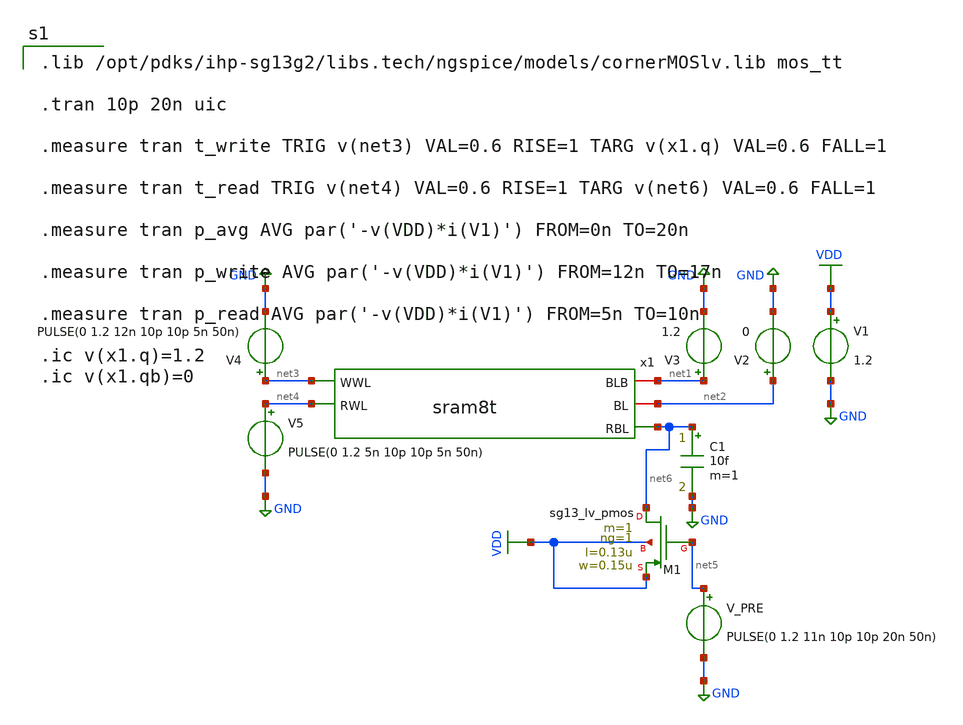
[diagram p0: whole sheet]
** sch_path: sram8t/schematic/sram8t_tb.sch
**.subckt sram8t_tb
V1 VDD GND 1.2
V3 net1 GND 1.2
V2 net2 GND 0
V4 net3 GND PULSE(0 1.2 12n 10p 10p 5n 50n)
V5 net4 GND PULSE(0 1.2 5n 10p 10p 5n 50n)
x1 net1 net2 net3 net6 net4 sram8t
XM1 net6 net5 VDD VDD sg13_lv_pmos w=0.15u l=0.13u ng=1 m=1 mm_ok=1
V_PRE net5 GND PULSE(0 1.2 11n 10p 10p 20n 50n)
C1 net6 GND 10f m=1
**** begin user architecture code

.lib /opt/pdks/ihp-sg13g2/libs.tech/ngspice/models/cornerMOSlv.lib mos_tt

.tran 10p 20n uic

.measure tran t_write TRIG v(net3) VAL=0.6 RISE=1 TARG v(x1.q) VAL=0.6 FALL=1

.measure tran t_read TRIG v(net4) VAL=0.6 RISE=1 TARG v(net6) VAL=0.6 FALL=1

.measure tran p_avg AVG par('-v(VDD)*i(V1)') FROM=0n TO=20n

.measure tran p_write AVG par('-v(VDD)*i(V1)') FROM=12n TO=17n

.measure tran p_read AVG par('-v(VDD)*i(V1)') FROM=5n TO=10n

.ic v(x1.q)=1.2
.ic v(x1.qb)=0

**** end user architecture code
**.ends

* expanding   symbol:  sram8t.sym # of pins=5
** sym_path: sram8t/schematic/sram8t.sym
** sch_path: sram8t/schematic/sram8t.sch
.subckt sram8t BLB BL WWL RBL RWL
*.iopin BL
*.iopin BLB
*.ipin WWL
*.ipin RWL
*.opin RBL
XM1 Q QB GND GND sg13_lv_nmos w=0.15u l=0.13u ng=1 m=1 mm_ok=1
XM2 QB Q GND GND sg13_lv_nmos w=0.15u l=0.13u ng=1 m=1 mm_ok=1
XM3 Q QB VDD VDD sg13_lv_pmos w=0.15u l=0.13u ng=1 m=1 mm_ok=1
XM4 QB Q VDD VDD sg13_lv_pmos w=0.15u l=0.13u ng=1 m=1 mm_ok=1
XM5 Q WWL BL GND sg13_lv_nmos w=0.15u l=0.13u ng=1 m=1 mm_ok=1
XM6 QB WWL BLB GND sg13_lv_nmos w=0.15u l=0.13u ng=1 m=1 mm_ok=1
XM7 RBL RWL net1 GND sg13_lv_nmos w=0.15u l=0.13u ng=1 m=1 mm_ok=1
XM8 net1 Q GND GND sg13_lv_nmos w=0.15u l=0.13u ng=1 m=1 mm_ok=1
.ends

.GLOBAL VDD
.GLOBAL GND
.end
